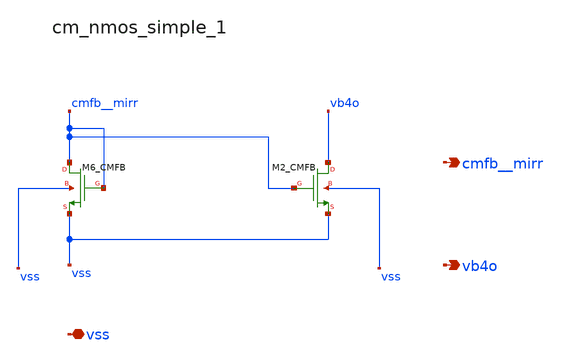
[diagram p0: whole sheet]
** sch_path: analog-db/raw/amp_034_fan_chopper_cmfb/hier/blocks/cm_nmos_simple_1.sch
**.subckt cm_nmos_simple_1 vss cmfb__mirr vb4o
*.iopin vss
*.opin cmfb__mirr
*.opin vb4o
XM2_CMFB vb4o cmfb__mirr vss vss sg13_lv_nmos w=x_dut_xm2_cmfb_w l=x_dut_xm2_cmfb_l ng=1
+ m=x_dut_xm2_cmfb_m
XM6_CMFB cmfb__mirr cmfb__mirr vss vss sg13_lv_nmos w=x_dut_xm6_cmfb_w l=x_dut_xm6_cmfb_l ng=1
+ m=x_dut_xm6_cmfb_m
**.ends
.end
